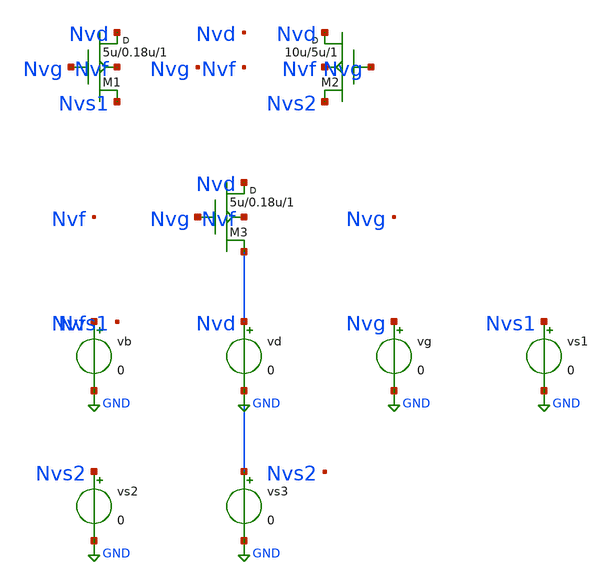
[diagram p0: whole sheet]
** sch_path: data/sch/aicas_MOS1_out.sch
**.subckt aicas_MOS1_out
vb Nvf GND 0
vd GND GND 0
vg Nvg GND 0
vs1 Nvs1 GND 0
vs2 Nvs2 GND 0
vs3 GND GND 0
M1 Nvd Nvg Nvs1 Nvf NMOS w=5u l=0.18u m=1
M2 Nvd Nvg Nvs2 Nvf NMOS w=10u l=5u m=1
M3 Nvd Nvg GND Nvf NMOS3 w=5u l=0.18u m=1
**.ends
.GLOBAL GND
.end
